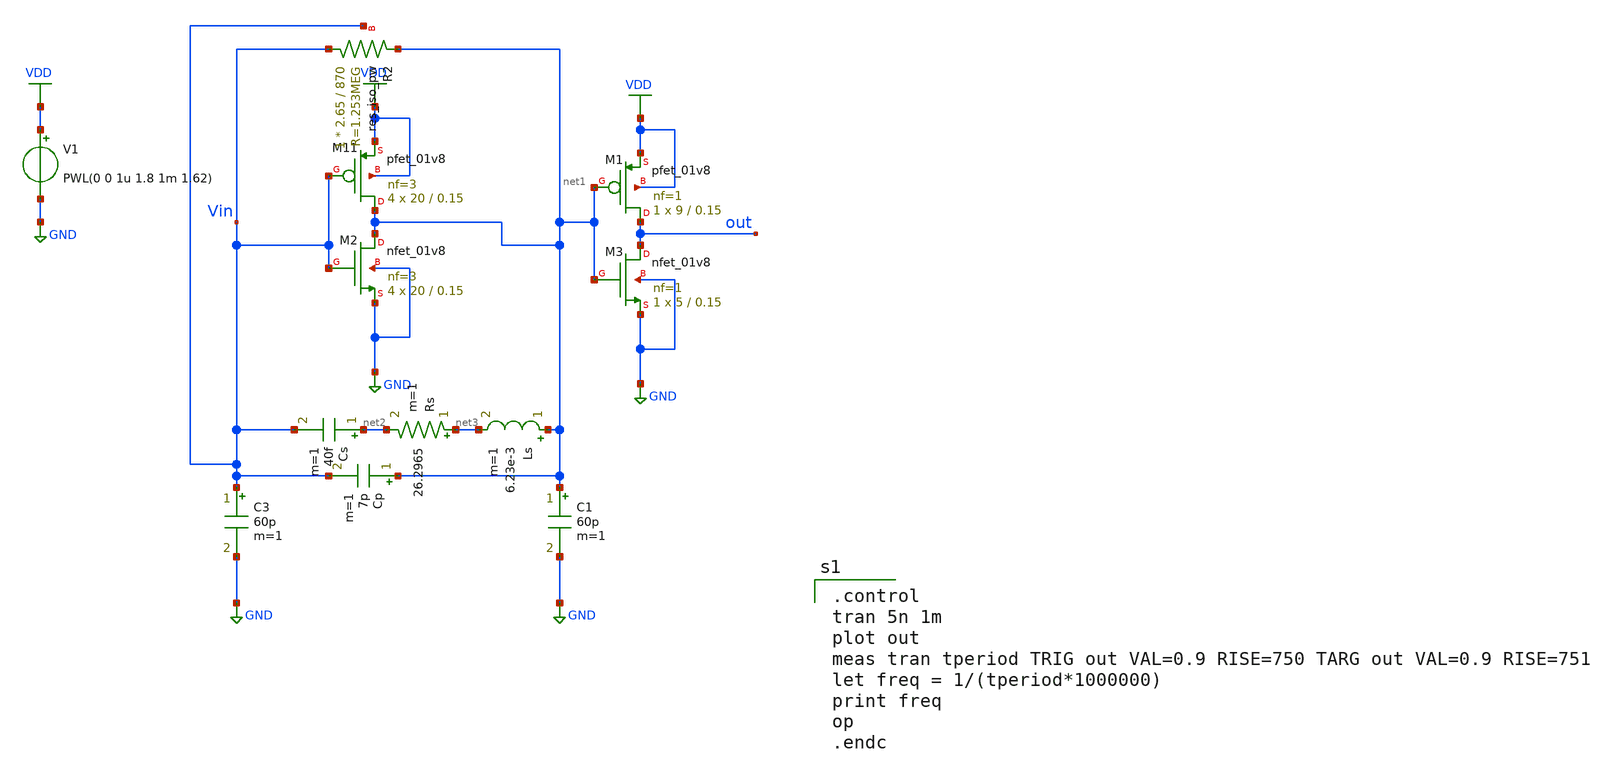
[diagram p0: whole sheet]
** sch_path: pll/xctl_lib/xctl/xschem/xctl.sch
**.subckt xctl
C1 net1 GND 60p m=1
C3 Vin GND 60p m=1
V1 VDD GND PWL(0 0 1u 1.8 1m 1.62)
Ls net1 net3 6.23e-3 m=1
Rs net3 net2 26.2965 m=1
Cs net2 Vin 40f m=1
Cp net1 Vin 7p m=1
XM11 net1 Vin VDD VDD sky130_fd_pr__pfet_01v8 L=0.15 W=20 nf=3 ad='int((nf+1)/2) * W/nf * 0.29' as='int((nf+2)/2) * W/nf * 0.29'
+ pd='2*int((nf+1)/2) * (W/nf + 0.29)' ps='2*int((nf+2)/2) * (W/nf + 0.29)' nrd='0.29 / W' nrs='0.29 / W'
+ sa=0 sb=0 sd=0 mult=4 m=4
XM2 net1 Vin GND GND sky130_fd_pr__nfet_01v8 L=0.15 W=20 nf=3 ad='int((3 + 1)/2) * 20 / 3 * 0.29' as='int((3 + 2)/2) * 20 / 3 * 0.29'
+ pd='2*int((3 + 1)/2) * (20 / 3 + 0.29)' ps='2*int((3 + 2)/2) * (20 / 3 + 0.29)' nrd='0.29 / 20 ' nrs='0.29 / 20 '
+ sa=0 sb=0 sd=0 mult=4 m=4
XM1 out net1 VDD VDD sky130_fd_pr__pfet_01v8 L=0.15 W=9 nf=1 ad='int((nf+1)/2) * W/nf * 0.29' as='int((nf+2)/2) * W/nf * 0.29'
+ pd='2*int((nf+1)/2) * (W/nf + 0.29)' ps='2*int((nf+2)/2) * (W/nf + 0.29)' nrd='0.29 / W' nrs='0.29 / W'
+ sa=0 sb=0 sd=0 mult=1 m=1
XM3 out net1 GND GND sky130_fd_pr__nfet_01v8 L=0.15 W=5 nf=1 ad='int((1 + 1)/2) * 5 / 1 * 0.29' as='int((1 + 2)/2) * 5 / 1 * 0.29'
+ pd='2*int((1 + 1)/2) * (5 / 1 + 0.29)' ps='2*int((1 + 2)/2) * (5 / 1 + 0.29)' nrd='0.29 / 5 ' nrs='0.29 / 5 '
+ sa=0 sb=0 sd=0 mult=1 m=1
XR2 Vin net1 Vin sky130_fd_pr__res_iso_pw W=2.65 L=870 m=1
**** begin user architecture code

** opencircuitdesign pdks install
.lib $::SKYWATER_MODELS/sky130.lib.spice tt



.control
tran 5n 1m
plot out
meas tran tperiod TRIG out VAL=0.9 RISE=750 TARG out VAL=0.9 RISE=751
let freq = 1/(tperiod*1000000)
print freq
op
.endc


**** end user architecture code
**.ends
.GLOBAL GND
.GLOBAL VDD
.end
